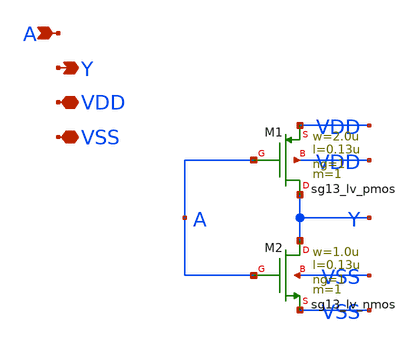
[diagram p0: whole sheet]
** sch_path: analog/xschem/inverter.sch
**.subckt inverter A Y VDD VSS
*.ipin A
*.opin Y
*.iopin VDD
*.iopin VSS
XM1 Y A VDD VDD sg13_lv_pmos w=2.0u l=0.13u ng=1 m=1 mm_ok=1
XM2 Y A VSS VSS sg13_lv_nmos w=1.0u l=0.13u ng=1 m=1 mm_ok=1
**.ends
.end
